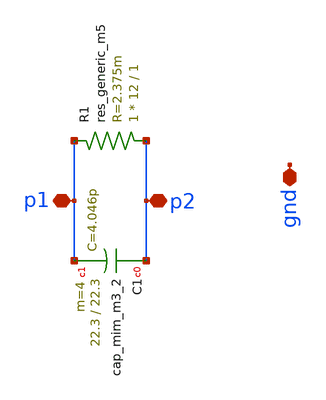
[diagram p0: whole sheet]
** sch_path: MICRO/lc_filter_lvs_xschem.sch
**.subckt lc_filter_lvs_xschem p2 p1 gnd
*.iopin p2
*.iopin p1
*.iopin gnd
XC1 p2 p1 sky130_fd_pr__cap_mim_m3_2 W=22.3 L=22.3 MF=4 m=4
R1 p2 p1 sky130_fd_pr__res_generic_m5 W=12 L=1 m=1
**.ends
.end
